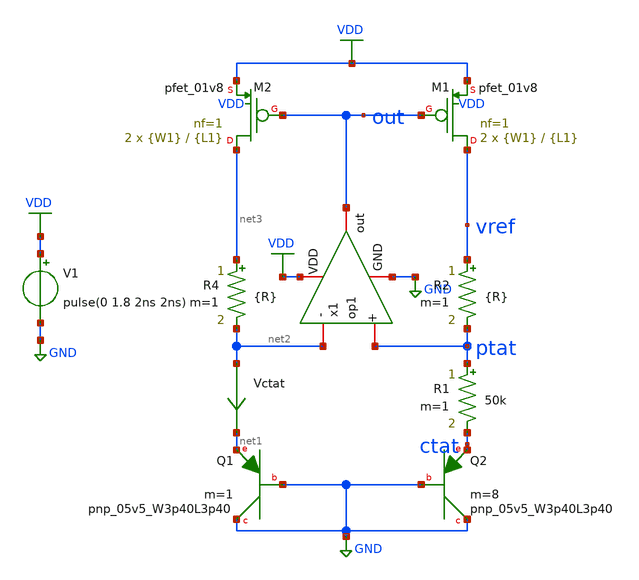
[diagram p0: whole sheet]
** sch_path: xschem/bgr_op2.sch
**.subckt bgr_op2
XQ1 GND GND net1 sky130_fd_pr__pnp_05v5_W3p40L3p40 m=1
XQ2 GND GND ctat sky130_fd_pr__pnp_05v5_W3p40L3p40 m=8
Vctat net2 net1 0
.save i(vctat)
V1 VDD GND pulse(0 1.8 2ns 2ns)
XM1 vref out VDD VDD sky130_fd_pr__pfet_01v8 L={L1} W={W1} nf=1 ad='int((nf+1)/2) * W/nf * 0.29' as='int((nf+2)/2) * W/nf * 0.29'
+ pd='2*int((nf+1)/2) * (W/nf + 0.29)' ps='2*int((nf+2)/2) * (W/nf + 0.29)' nrd='0.29 / W' nrs='0.29 / W'
+ sa=0 sb=0 sd=0 mult=2 m=2
XM2 net3 out VDD VDD sky130_fd_pr__pfet_01v8 L={L1} W={W1} nf=1 ad='int((nf+1)/2) * W/nf * 0.29' as='int((nf+2)/2) * W/nf * 0.29'
+ pd='2*int((nf+1)/2) * (W/nf + 0.29)' ps='2*int((nf+2)/2) * (W/nf + 0.29)' nrd='0.29 / W' nrs='0.29 / W'
+ sa=0 sb=0 sd=0 mult=2 m=2
R1 ptat ctat 50k m=1
R2 vref ptat {R} m=1
R4 net3 net2 {R} m=1
x1 VDD out net2 ptat GND op1
**** begin user architecture code


.param L1=0.15
.param W1=1
.param R=489k



** opencircuitdesign pdks install
.lib $::SKYWATER_MODELS/sky130.lib.spice tt




.option savecurrents
.control
save all
op
remzerovec
write bgr_op2.raw
set appendwrite

dc temp -40 85 1
show >bgr_op2.lis
remzerovec
write bgr_op2.raw
plot (ptat-ctat)
plot ctat
plot vref

********TC********
meas dc temp_avg_vref avg v(vref)
meas dc temp_vref_27 find v(vref) when temp-sweep=27
meas dc temp_pp_vref PP v(vref)
meas dc temp_vref_max max v(vref)
meas dc temp_max_vref when v(vref)='temp_vref_max'
meas dc temp_vref_min min v(vref)
meas dc temp_min_vref when v(vref)='temp_vref_min'
let vref_tc='((temp_pp_vref*1000000)/(125*temp_avg_vref))'
print vref_tc

******PSRR******
ac dec 1000 1 10Meg
write bgr_op2.raw
remzerovec
plot vdb(vref)
write bgr_op2.ac vdb(vref)
meas ac psrr find vdb(vref) at=1k

****Power****
tran 10us 100ms
write bgr_op2.raw
remzerovec
meas tran ave_v avg vdd
meas tran ave_i avg i(v1)
let ave_power='ave_v*(-ave_i)
plot vdd vref
*plot -i(v1)
print ave_power

*******LS******
dc v1 0 3.5 0.1
write bgr_op2.raw
remzerovec
plot vdd vref
meas dc vref_max max v(vref) from=1.62 to=1.98
meas dc vref_min min v(vref) from=1.62 to=1.98
let ls='100*(vref_max-vref_min)/vref_min/(1.98-1.62)'
print ls

.endc


**** end user architecture code
**.ends

* expanding   symbol:  op1.sym # of pins=5
** sym_path: xschem/op1.sym
** sch_path: xschem/op1.sch
.subckt op1 VDD out - + GND
*.iopin VDD
*.iopin GND
*.iopin -
*.iopin +
*.iopin out
**** begin user architecture code


.param L=20
.param W=1


**** end user architecture code
C2 out net5 2.2p m=1
R2 net5 net1 850k m=1
XM1 bias bias GND GND sky130_fd_pr__nfet_01v8 L={L} W={W/1.5} nf=1 ad='int((nf+1)/2) * W/nf * 0.29' as='int((nf+2)/2)
+ * W/nf * 0.29' pd='2*int((nf+1)/2) * (W/nf + 0.29)' ps='2*int((nf+2)/2) * (W/nf + 0.29)' nrd='0.29 /
+ W' nrs='0.29 / W' sa=0 sb=0 sd=0 mult=2 m=2
XM2 net4 bias GND GND sky130_fd_pr__nfet_01v8 L={L} W={W/1.5} nf=1 ad='int((nf+1)/2) * W/nf * 0.29' as='int((nf+2)/2)
+ * W/nf * 0.29' pd='2*int((nf+1)/2) * (W/nf + 0.29)' ps='2*int((nf+2)/2) * (W/nf + 0.29)' nrd='0.29 /
+ W' nrs='0.29 / W' sa=0 sb=0 sd=0 mult=2 m=2
XM3 net2 - net3 GND sky130_fd_pr__nfet_01v8 L={L} W={W} nf=1 ad='int((nf+1)/2) * W/nf * 0.29' as='int((nf+2)/2)
+ * W/nf * 0.29' pd='2*int((nf+1)/2) * (W/nf + 0.29)' ps='2*int((nf+2)/2) * (W/nf + 0.29)' nrd='0.29 /
+ W' nrs='0.29 / W' sa=0 sb=0 sd=0 mult=4 m=4
XM4 net1 + net3 GND sky130_fd_pr__nfet_01v8 L={L} W={W} nf=1 ad='int((nf+1)/2) * W/nf * 0.29' as='int((nf+2)/2)
+ * W/nf * 0.29' pd='2*int((nf+1)/2) * (W/nf + 0.29)' ps='2*int((nf+2)/2) * (W/nf + 0.29)' nrd='0.29 /
+ W' nrs='0.29 / W' sa=0 sb=0 sd=0 mult=4 m=4
XM6 bias net4 VDD VDD sky130_fd_pr__pfet_01v8 L={L} W={W/1.5} nf=1 ad='int((nf+1)/2) * W/nf * 0.29' as='int((nf+2)/2)
+ * W/nf * 0.29' pd='2*int((nf+1)/2) * (W/nf + 0.29)' ps='2*int((nf+2)/2) * (W/nf + 0.29)' nrd='0.29 /
+ W' nrs='0.29 / W' sa=0 sb=0 sd=0 mult=2 m=2
XM7 net4 net4 VDD VDD sky130_fd_pr__pfet_01v8 L={L} W={W/1.5} nf=1 ad='int((nf+1)/2) * W/nf * 0.29' as='int((nf+2)/2)
+ * W/nf * 0.29' pd='2*int((nf+1)/2) * (W/nf + 0.29)' ps='2*int((nf+2)/2) * (W/nf + 0.29)' nrd='0.29 /
+ W' nrs='0.29 / W' sa=0 sb=0 sd=0 mult=2 m=2
XM8 net1 net2 VDD VDD sky130_fd_pr__pfet_01v8 L={L} W={W} nf=1 ad='int((nf+1)/2) * W/nf * 0.29' as='int((nf+2)/2)
+ * W/nf * 0.29' pd='2*int((nf+1)/2) * (W/nf + 0.29)' ps='2*int((nf+2)/2) * (W/nf + 0.29)' nrd='0.29 /
+ W' nrs='0.29 / W' sa=0 sb=0 sd=0 mult=4 m=4
XM9 net2 net2 VDD VDD sky130_fd_pr__pfet_01v8 L={L} W={W} nf=1 ad='int((nf+1)/2) * W/nf * 0.29' as='int((nf+2)/2)
+ * W/nf * 0.29' pd='2*int((nf+1)/2) * (W/nf + 0.29)' ps='2*int((nf+2)/2) * (W/nf + 0.29)' nrd='0.29 /
+ W' nrs='0.29 / W' sa=0 sb=0 sd=0 mult=4 m=4
XM5 net3 bias GND GND sky130_fd_pr__nfet_01v8 L={L} W={W} nf=1 ad='int((nf+1)/2) * W/nf * 0.29' as='int((nf+2)/2)
+ * W/nf * 0.29' pd='2*int((nf+1)/2) * (W/nf + 0.29)' ps='2*int((nf+2)/2) * (W/nf + 0.29)' nrd='0.29 /
+ W' nrs='0.29 / W' sa=0 sb=0 sd=0 mult=4 m=4
XM10 out net1 VDD VDD sky130_fd_pr__pfet_01v8 L={L} W={W*1.1} nf=1 ad='int((nf+1)/2) * W/nf * 0.29' as='int((nf+2)/2)
+ * W/nf * 0.29' pd='2*int((nf+1)/2) * (W/nf + 0.29)' ps='2*int((nf+2)/2) * (W/nf + 0.29)' nrd='0.29 /
+ W' nrs='0.29 / W' sa=0 sb=0 sd=0 mult=4 m=4
XM11 out bias GND GND sky130_fd_pr__nfet_01v8 L={L} W={W} nf=1 ad='int((nf+1)/2) * W/nf * 0.29' as='int((nf+2)/2)
+ * W/nf * 0.29' pd='2*int((nf+1)/2) * (W/nf + 0.29)' ps='2*int((nf+2)/2) * (W/nf + 0.29)' nrd='0.29 /
+ W' nrs='0.29 / W' sa=0 sb=0 sd=0 mult=2 m=2
.ends

.GLOBAL VDD
.GLOBAL GND
.end
